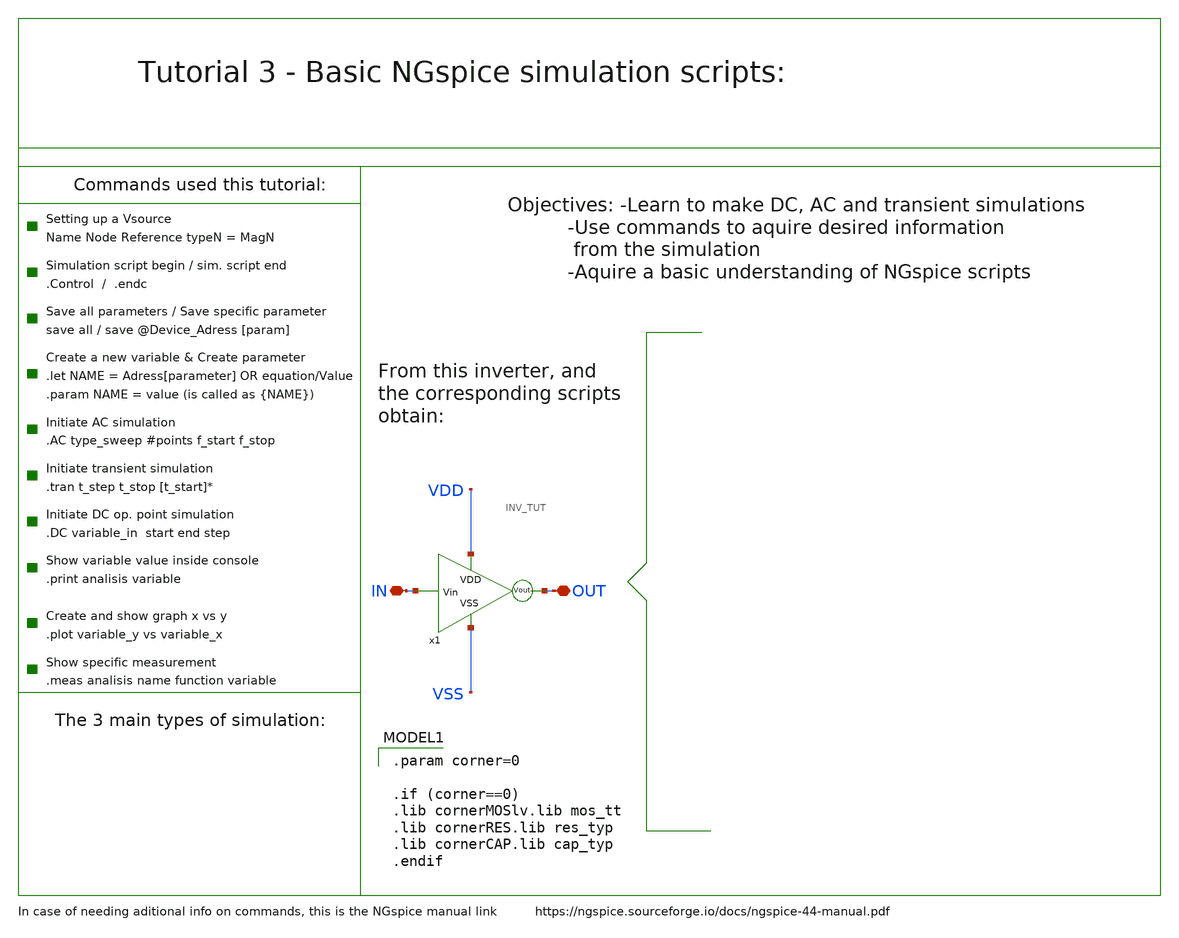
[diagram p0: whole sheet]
** sch_path: Tutoriales/Tutorial_3.sch
**.subckt Tutorial_3 IN OUT
*.iopin IN
*.iopin OUT
x1 VSS VDD OUT IN INV_TUT
**** begin user architecture code



vvdd vdd 0 dc 1.8
vvss vss 0 0
VSINE IN 0  SIN(0.9 0.9 1e6 0 0 0)
cload vout 0 5p

.control
save all
tran 0.1n 10u
plot v(OUT) v(IN)
.endc


.end


 .param corner=0

.if (corner==0)
.lib cornerMOSlv.lib mos_tt
.lib cornerRES.lib res_typ
.lib cornerCAP.lib cap_typ
.endif

**** end user architecture code
**.ends

* expanding   symbol:  /foss/designs/Tutoriales_Xschem/Tutoriales/INV_TUT.sym # of pins=4
** sym_path: Tutoriales/INV_TUT.sym
** sch_path: Tutoriales/INV_TUT.sch
.subckt INV_TUT VSS VDD Vout Vin
*.ipin Vin
*.opin Vout
*.ipin VSS
*.ipin VDD
XM1 Vout Vin VSS VSS sg13_lv_nmos w=0.15u l=0.13u ng=1 m=1 mm_ok=1
XM2 Vout Vin VDD VDD sg13_lv_pmos w=0.45u l=0.13u ng=1 m=1 mm_ok=1
.ends

.end
